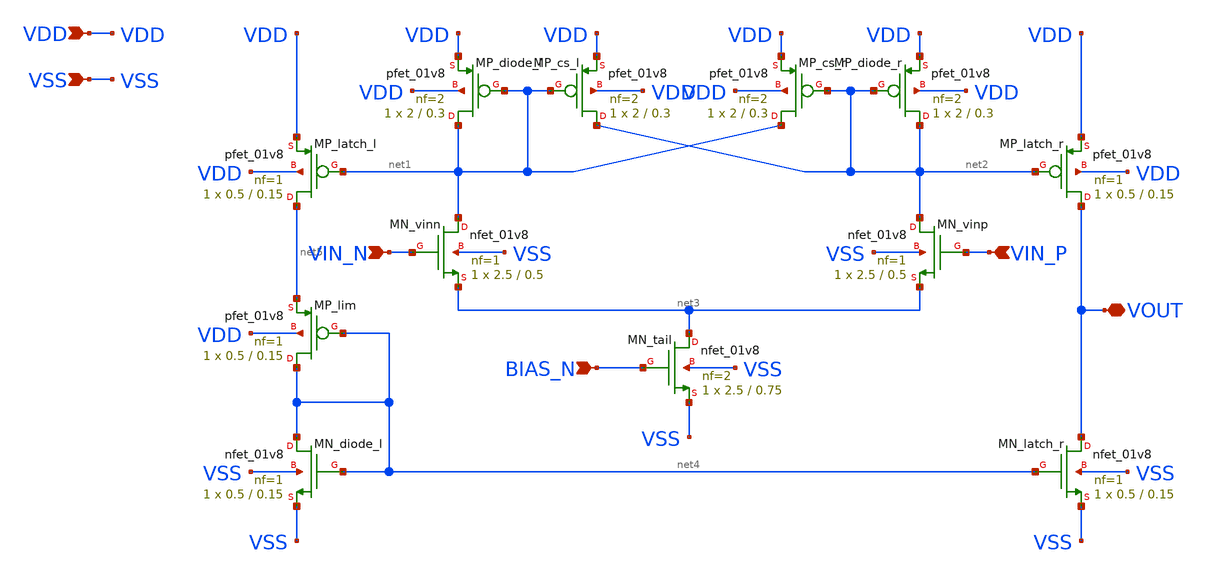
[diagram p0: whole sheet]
** sch_path: schem/symbol_repo/sym_comp_n.sch
**.subckt sym_comp_n VDD VSS VIN_N VIN_P BIAS_N VOUT
*.ipin VDD
*.ipin VSS
*.ipin VIN_N
*.ipin VIN_P
*.ipin BIAS_N
*.iopin VOUT
XMP_diode_l net1 net1 VDD VDD sky130_fd_pr__pfet_01v8 L=0.3 W=2 nf=2 ad='int((2 + 1)/2) * 2 / 2 * 0.29'
+ as='int((2 + 2)/2) * 2 / 2 * 0.29' pd='2*int((2 + 1)/2) * (2 / 2 + 0.29)' ps='2*int((2 + 2)/2) * (2 / 2 + 0.29)'
+ nrd='0.29 / 2 ' nrs='0.29 / 2 ' sa=0 sb=0 sd=0 mult=1 m=1
XMP_cs_l net2 net1 VDD VDD sky130_fd_pr__pfet_01v8 L=0.3 W=2 nf=2 ad='int((2 + 1)/2) * 2 / 2 * 0.29'
+ as='int((2 + 2)/2) * 2 / 2 * 0.29' pd='2*int((2 + 1)/2) * (2 / 2 + 0.29)' ps='2*int((2 + 2)/2) * (2 / 2 + 0.29)'
+ nrd='0.29 / 2 ' nrs='0.29 / 2 ' sa=0 sb=0 sd=0 mult=1 m=1
XMP_cs_r net1 net2 VDD VDD sky130_fd_pr__pfet_01v8 L=0.3 W=2 nf=2 ad='int((2 + 1)/2) * 2 / 2 * 0.29'
+ as='int((2 + 2)/2) * 2 / 2 * 0.29' pd='2*int((2 + 1)/2) * (2 / 2 + 0.29)' ps='2*int((2 + 2)/2) * (2 / 2 + 0.29)'
+ nrd='0.29 / 2 ' nrs='0.29 / 2 ' sa=0 sb=0 sd=0 mult=1 m=1
XMP_diode_r net2 net2 VDD VDD sky130_fd_pr__pfet_01v8 L=0.3 W=2 nf=2 ad='int((2 + 1)/2) * 2 / 2 * 0.29'
+ as='int((2 + 2)/2) * 2 / 2 * 0.29' pd='2*int((2 + 1)/2) * (2 / 2 + 0.29)' ps='2*int((2 + 2)/2) * (2 / 2 + 0.29)'
+ nrd='0.29 / 2 ' nrs='0.29 / 2 ' sa=0 sb=0 sd=0 mult=1 m=1
XMN_vinn net1 VIN_N net3 VSS sky130_fd_pr__nfet_01v8 L=0.5 W=2.5 nf=1 ad='int((1 + 1)/2) * 2.5 / 1 * 0.29'
+ as='int((1 + 2)/2) * 2.5 / 1 * 0.29' pd='2*int((1 + 1)/2) * (2.5 / 1 + 0.29)' ps='2*int((1 + 2)/2) * (2.5 / 1 + 0.29)'
+ nrd='0.29 / 2.5 ' nrs='0.29 / 2.5 ' sa=0 sb=0 sd=0 mult=1 m=1
XMN_vinp net2 VIN_P net3 VSS sky130_fd_pr__nfet_01v8 L=0.5 W=2.5 nf=1 ad='int((1 + 1)/2) * 2.5 / 1 * 0.29'
+ as='int((1 + 2)/2) * 2.5 / 1 * 0.29' pd='2*int((1 + 1)/2) * (2.5 / 1 + 0.29)' ps='2*int((1 + 2)/2) * (2.5 / 1 + 0.29)'
+ nrd='0.29 / 2.5 ' nrs='0.29 / 2.5 ' sa=0 sb=0 sd=0 mult=1 m=1
XMN_tail net3 BIAS_N VSS VSS sky130_fd_pr__nfet_01v8 L=0.75 W=2.5 nf=2 ad='int((2 + 1)/2) * 2.5 / 2 * 0.29'
+ as='int((2 + 2)/2) * 2.5 / 2 * 0.29' pd='2*int((2 + 1)/2) * (2.5 / 2 + 0.29)' ps='2*int((2 + 2)/2) * (2.5 / 2 + 0.29)'
+ nrd='0.29 / 2.5 ' nrs='0.29 / 2.5 ' sa=0 sb=0 sd=0 mult=1 m=1
XMP_latch_r VOUT net2 VDD VDD sky130_fd_pr__pfet_01v8 L=0.15 W=0.5 nf=1 ad='int((1 + 1)/2) * 0.5 / 1 * 0.29'
+ as='int((1 + 2)/2) * 0.5 / 1 * 0.29' pd='2*int((1 + 1)/2) * (0.5 / 1 + 0.29)' ps='2*int((1 + 2)/2) * (0.5 / 1 + 0.29)'
+ nrd='0.29 / 0.5 ' nrs='0.29 / 0.5 ' sa=0 sb=0 sd=0 mult=1 m=1
XMP_latch_l net5 net1 VDD VDD sky130_fd_pr__pfet_01v8 L=0.15 W=0.5 nf=1 ad='int((1 + 1)/2) * 0.5 / 1 * 0.29'
+ as='int((1 + 2)/2) * 0.5 / 1 * 0.29' pd='2*int((1 + 1)/2) * (0.5 / 1 + 0.29)' ps='2*int((1 + 2)/2) * (0.5 / 1 + 0.29)'
+ nrd='0.29 / 0.5 ' nrs='0.29 / 0.5 ' sa=0 sb=0 sd=0 mult=1 m=1
XMN_latch_r VOUT net4 VSS VSS sky130_fd_pr__nfet_01v8 L=0.15 W=0.5 nf=1 ad='int((1 + 1)/2) * 0.5 / 1 * 0.29'
+ as='int((1 + 2)/2) * 0.5 / 1 * 0.29' pd='2*int((1 + 1)/2) * (0.5 / 1 + 0.29)' ps='2*int((1 + 2)/2) * (0.5 / 1 + 0.29)'
+ nrd='0.29 / 0.5 ' nrs='0.29 / 0.5 ' sa=0 sb=0 sd=0 mult=1 m=1
XMN_diode_l net4 net4 VSS VSS sky130_fd_pr__nfet_01v8 L=0.15 W=0.5 nf=1 ad='int((1 + 1)/2) * 0.5 / 1 * 0.29'
+ as='int((1 + 2)/2) * 0.5 / 1 * 0.29' pd='2*int((1 + 1)/2) * (0.5 / 1 + 0.29)' ps='2*int((1 + 2)/2) * (0.5 / 1 + 0.29)'
+ nrd='0.29 / 0.5 ' nrs='0.29 / 0.5 ' sa=0 sb=0 sd=0 mult=1 m=1
XMP_lim net4 net4 net5 VDD sky130_fd_pr__pfet_01v8 L=0.15 W=0.5 nf=1 ad='int((1 + 1)/2) * 0.5 / 1 * 0.29'
+ as='int((1 + 2)/2) * 0.5 / 1 * 0.29' pd='2*int((1 + 1)/2) * (0.5 / 1 + 0.29)' ps='2*int((1 + 2)/2) * (0.5 / 1 + 0.29)'
+ nrd='0.29 / 0.5 ' nrs='0.29 / 0.5 ' sa=0 sb=0 sd=0 mult=1 m=1
**.ends
.end
